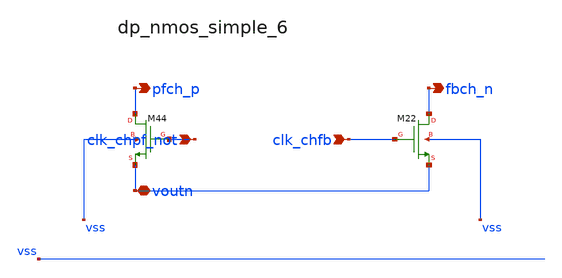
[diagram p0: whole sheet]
** sch_path: analog-db/raw/ia_003_fan_chopper_pf/hier/blocks/dp_nmos_simple_6.sch
**.subckt dp_nmos_simple_6 clk_chpf_not clk_chfb voutn pfch_p fbch_n
*.ipin clk_chpf_not
*.ipin clk_chfb
*.iopin voutn
*.opin pfch_p
*.opin fbch_n
XM22 fbch_n clk_chfb voutn vss sg13_lv_nmos w=x_dut_xm22_w l=x_dut_xm22_l ng=1 m=x_dut_xm22_m
XM44 pfch_p clk_chpf_not voutn vss sg13_lv_nmos w=x_dut_xm44_w l=x_dut_xm44_l ng=1 m=x_dut_xm44_m
**.ends
.end
